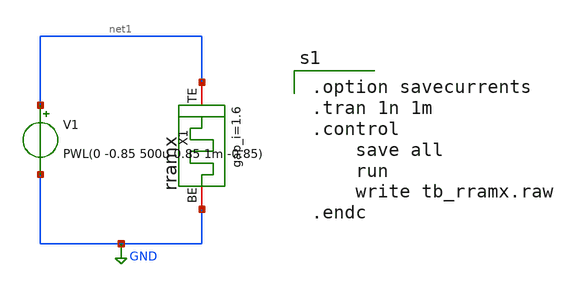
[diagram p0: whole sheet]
** sch_path: designs/tb_memristor/tb_rramx.sch
**.subckt tb_rramx
V1 net1 GND PWL(0 -0.85 500u 0.85 1m -0.85)
.save i(v1)
X1 net1 GND rram_cell gap_i=1.6
**** begin user architecture code

.option savecurrents
.tran 1n 1m
.control
	save all
	run
	write tb_rramx.raw
.endc


.subckt rram_cell BE TE gap_i=0.1
N1 BE TE rram_model
.model rram_model rram gap_initial={gap_i}
.ends rram_cell

.control
pre_osdi /foss/designs/spike_130/designs/prubs/rram.osdi
.endc

**** end user architecture code
**.ends
.GLOBAL GND
.end
